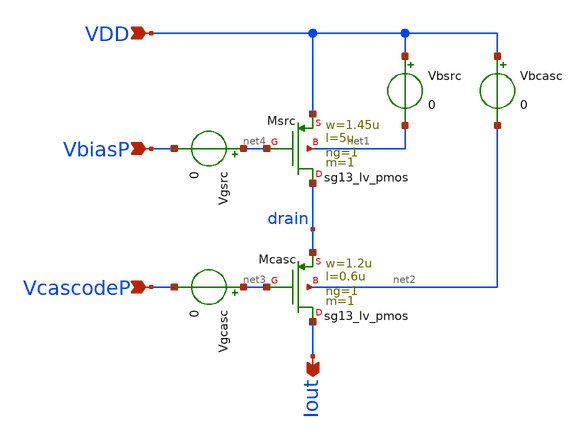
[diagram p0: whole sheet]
** sch_path: xschem/pcsource2u.sch
**.subckt pcsource2u VcascodeP VbiasP Iout VDD
*.ipin VcascodeP
*.ipin VbiasP
*.opin Iout
*.ipin VDD
XMsrc drain net4 VDD net1 sg13_lv_pmos w=1.45u l=5u ng=1 m=1 mm_ok=1
XMcasc Iout net3 drain net2 sg13_lv_pmos w=1.2u l=0.6u ng=1 m=1 mm_ok=1
Vgsrc net4 VbiasP 0
.save i(vgsrc)
Vgcasc net3 VcascodeP 0
.save i(vgcasc)
Vbsrc VDD net1 0
.save i(vbsrc)
Vbcasc VDD net2 0
.save i(vbcasc)
**.ends
.end
